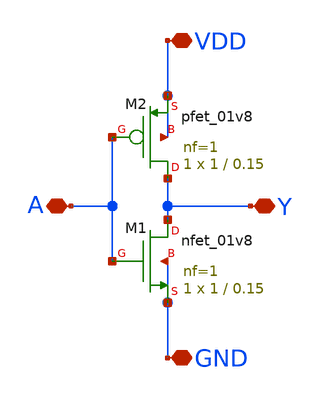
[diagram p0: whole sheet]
** sch_path: magic_tut/xschem/inverter.sch
**.subckt inverter VDD GND Y A
*.iopin VDD
*.iopin GND
*.iopin Y
*.iopin A
XM1 Y A GND GND sky130_fd_pr__nfet_01v8 L=0.15 W=1 nf=1 ad='int((nf+1)/2) * W/nf * 0.29' as='int((nf+2)/2) * W/nf * 0.29'
+ pd='2*int((nf+1)/2) * (W/nf + 0.29)' ps='2*int((nf+2)/2) * (W/nf + 0.29)' nrd='0.29 / W' nrs='0.29 / W'
+ sa=0 sb=0 sd=0 mult=1 m=1
XM2 Y A VDD VDD sky130_fd_pr__pfet_01v8 L=0.15 W=1 nf=1 ad='int((nf+1)/2) * W/nf * 0.29' as='int((nf+2)/2) * W/nf * 0.29'
+ pd='2*int((nf+1)/2) * (W/nf + 0.29)' ps='2*int((nf+2)/2) * (W/nf + 0.29)' nrd='0.29 / W' nrs='0.29 / W'
+ sa=0 sb=0 sd=0 mult=1 m=1
**.ends
.end
